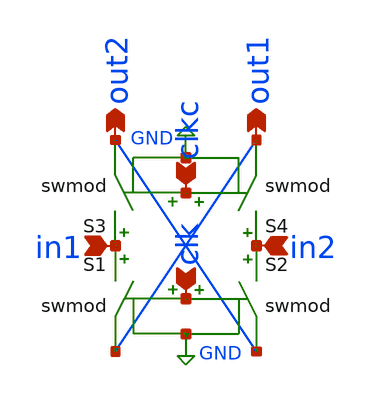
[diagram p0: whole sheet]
** sch_path: idealchopper.sch
**.subckt idealchopper in1 in2 out2 out1 clkc clk
*.ipin in1
*.ipin in2
*.opin out2
*.opin out1
*.ipin clkc
*.ipin clk
S1 in1 out1 clk GND swmod
S2 in2 out2 clk GND swmod
S3 in1 out2 clkc GND swmod
S4 in2 out1 clkc GND swmod
**.ends
.GLOBAL GND
.end
